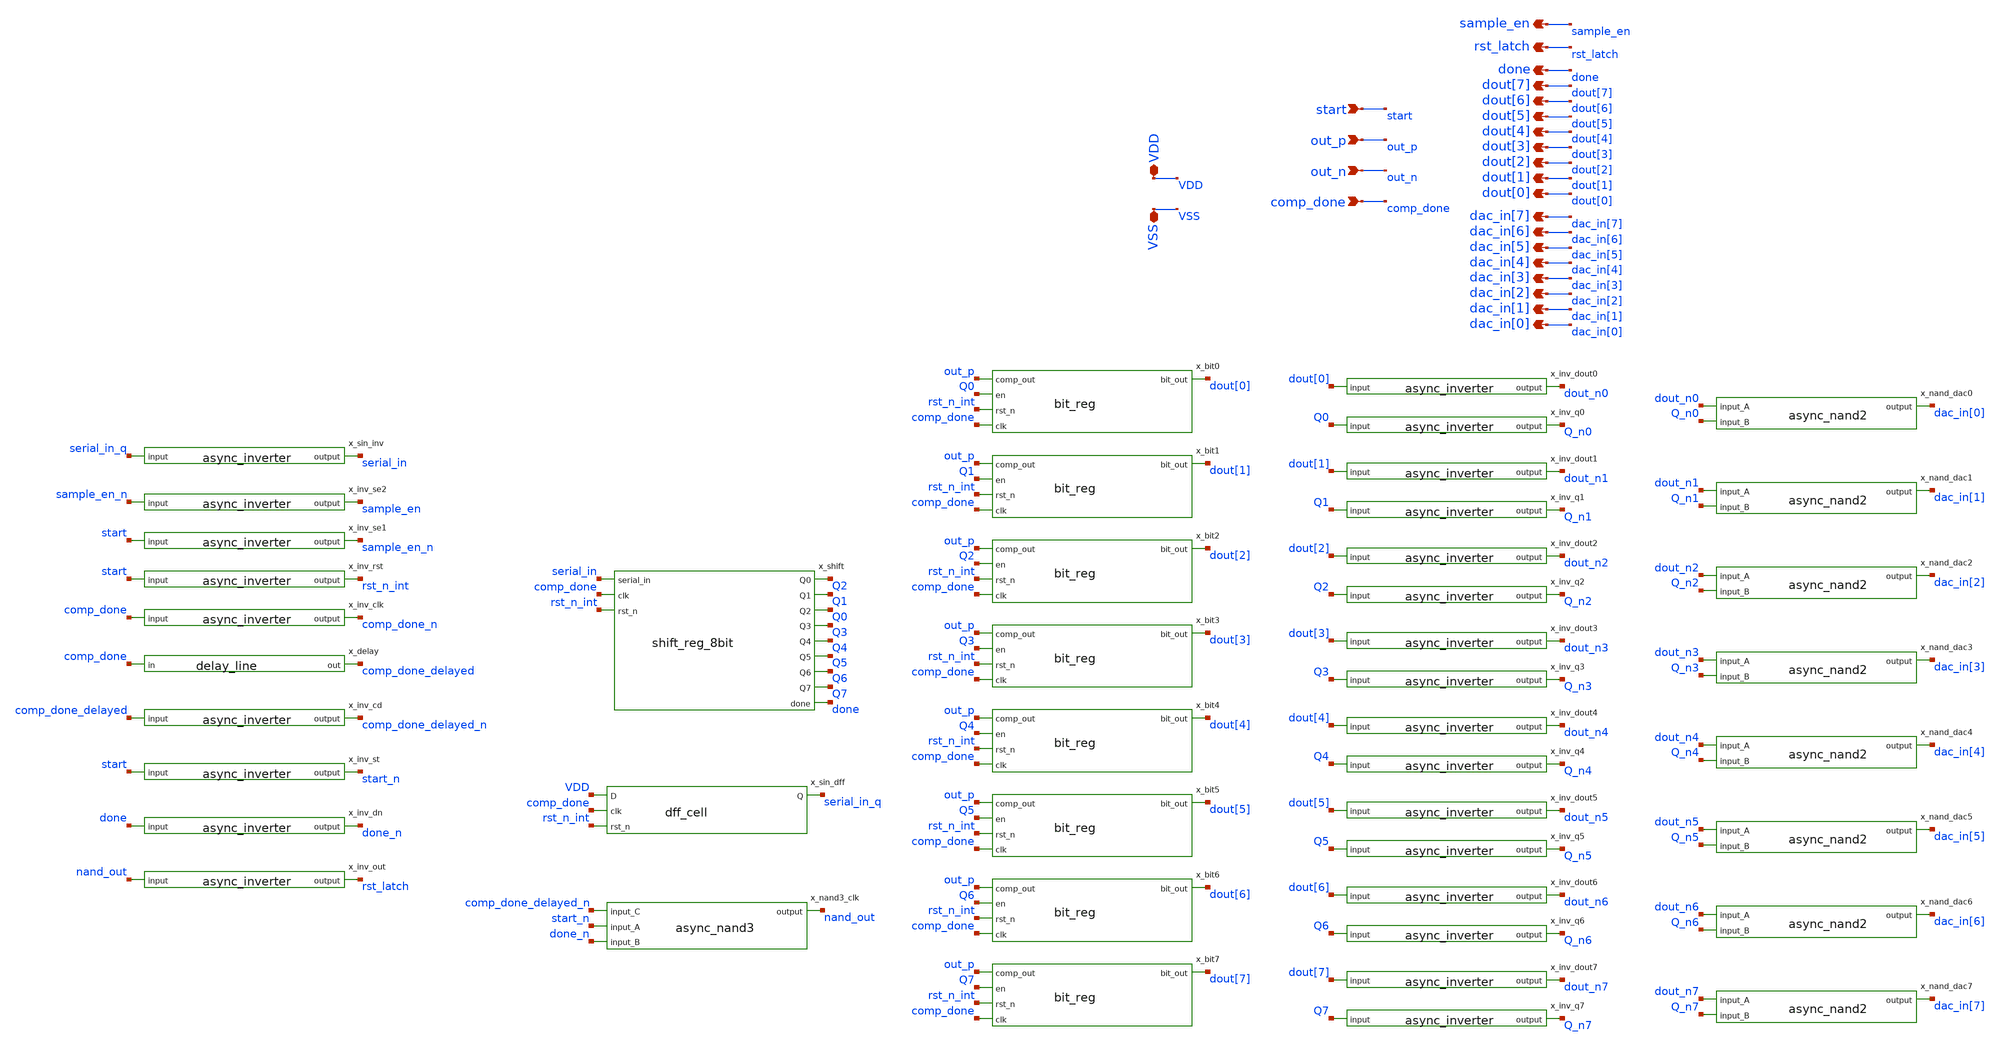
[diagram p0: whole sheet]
** sch_path: xschem/sar_adc/async_sar.sch
**.subckt async_sar start out_p out_n comp_done VDD VSS sample_en rst_latch done dout[0] dac_in[0]
*+ dout[1] dac_in[1] dout[2] dac_in[2] dout[3] dac_in[3] dout[4] dac_in[4] dout[5] dac_in[5] dout[6] dac_in[6]
*+ dout[7] dac_in[7]
*.ipin start
*.ipin out_p
*.ipin out_n
*.ipin comp_done
*.iopin VDD
*.iopin VSS
*.opin sample_en
*.opin rst_latch
*.opin done
*.opin dout[0]
*.opin dac_in[0]
*.opin dout[1]
*.opin dac_in[1]
*.opin dout[2]
*.opin dac_in[2]
*.opin dout[3]
*.opin dac_in[3]
*.opin dout[4]
*.opin dac_in[4]
*.opin dout[5]
*.opin dac_in[5]
*.opin dout[6]
*.opin dac_in[6]
*.opin dout[7]
*.opin dac_in[7]
x_inv_rst start rst_n_int async_inverter
x_inv_clk comp_done comp_done_n async_inverter
x_inv_se1 start sample_en_n async_inverter
x_inv_se2 sample_en_n sample_en async_inverter
x_sin_dff VDD comp_done rst_n_int serial_in_q dff_cell
x_sin_inv serial_in_q serial_in async_inverter
x_shift serial_in comp_done rst_n_int Q2 Q1 Q0 Q3 Q4 Q5 Q6 Q7 done shift_reg_8bit
x_bit0 out_p dout[0] Q0 rst_n_int comp_done bit_reg
x_bit1 out_p dout[1] Q1 rst_n_int comp_done bit_reg
x_bit2 out_p dout[2] Q2 rst_n_int comp_done bit_reg
x_bit3 out_p dout[3] Q3 rst_n_int comp_done bit_reg
x_bit4 out_p dout[4] Q4 rst_n_int comp_done bit_reg
x_bit5 out_p dout[5] Q5 rst_n_int comp_done bit_reg
x_bit6 out_p dout[6] Q6 rst_n_int comp_done bit_reg
x_bit7 out_p dout[7] Q7 rst_n_int comp_done bit_reg
x_delay comp_done_delayed comp_done delay_line
x_inv_cd comp_done_delayed comp_done_delayed_n async_inverter
x_inv_st start start_n async_inverter
x_inv_dn done done_n async_inverter
x_nand3_clk comp_done_delayed_n start_n done_n nand_out async_nand3
x_inv_out nand_out rst_latch async_inverter
x_inv_dout0 dout[0] dout_n0 async_inverter
x_inv_q0 Q0 Q_n0 async_inverter
x_nand_dac0 dout_n0 dac_in[0] Q_n0 async_nand2
x_inv_dout1 dout[1] dout_n1 async_inverter
x_inv_q1 Q1 Q_n1 async_inverter
x_nand_dac1 dout_n1 dac_in[1] Q_n1 async_nand2
x_inv_dout2 dout[2] dout_n2 async_inverter
x_inv_q2 Q2 Q_n2 async_inverter
x_nand_dac2 dout_n2 dac_in[2] Q_n2 async_nand2
x_inv_dout3 dout[3] dout_n3 async_inverter
x_inv_q3 Q3 Q_n3 async_inverter
x_nand_dac3 dout_n3 dac_in[3] Q_n3 async_nand2
x_inv_dout4 dout[4] dout_n4 async_inverter
x_inv_q4 Q4 Q_n4 async_inverter
x_nand_dac4 dout_n4 dac_in[4] Q_n4 async_nand2
x_inv_dout5 dout[5] dout_n5 async_inverter
x_inv_q5 Q5 Q_n5 async_inverter
x_nand_dac5 dout_n5 dac_in[5] Q_n5 async_nand2
x_inv_dout6 dout[6] dout_n6 async_inverter
x_inv_q6 Q6 Q_n6 async_inverter
x_nand_dac6 dout_n6 dac_in[6] Q_n6 async_nand2
x_inv_dout7 dout[7] dout_n7 async_inverter
x_inv_q7 Q7 Q_n7 async_inverter
x_nand_dac7 dout_n7 dac_in[7] Q_n7 async_nand2
**.ends
.end
